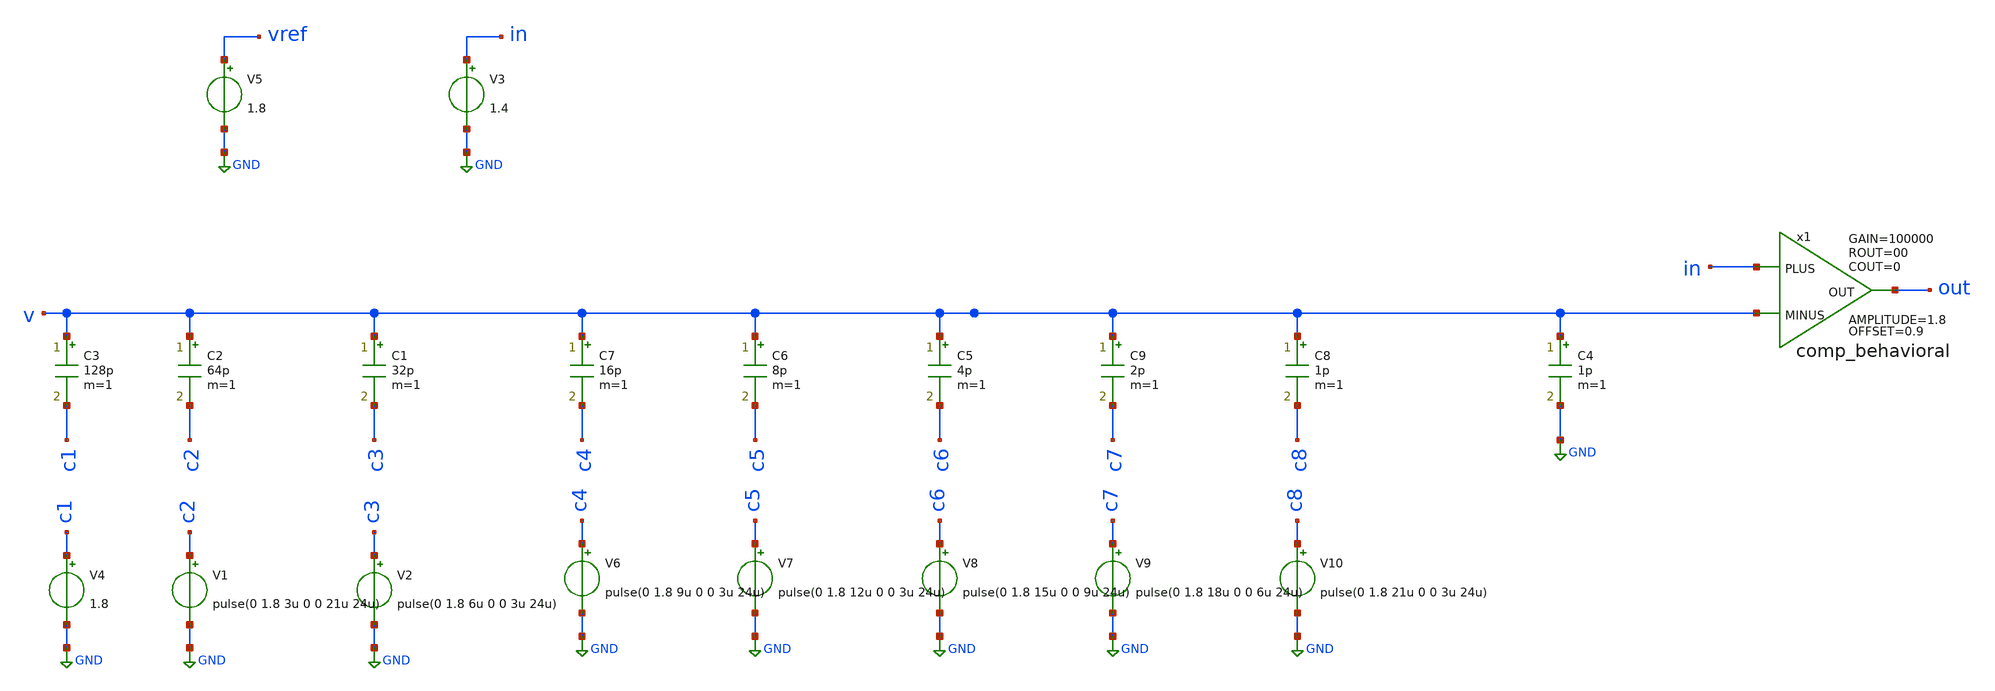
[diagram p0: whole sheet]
** sch_path: Behavioral_model/S_SARADC.sch
**.subckt S_SARADC
x1 in v out comp_behavioral OFFSET=0.9 AMPLITUDE=1.8 GAIN=100000 ROUT=00 COUT=0
V3 in GND 1.4
V4 c1 GND 1.8
C1 v c3 32p m=1
C2 v c2 64p m=1
C3 v c1 128p m=1
C4 v GND 1p m=1
V1 c2 GND pulse(0 1.8 3u 0 0 21u 24u)
V2 c3 GND pulse(0 1.8 6u 0 0 3u 24u)
V5 vref GND 1.8
C5 v c6 4p m=1
C6 v c5 8p m=1
C7 v c4 16p m=1
C8 v c8 1p m=1
C9 v c7 2p m=1
V6 c4 GND pulse(0 1.8 9u 0 0 3u 24u)
V7 c5 GND pulse(0 1.8 12u 0 0 3u 24u)
V8 c6 GND pulse(0 1.8 15u 0 0 9u 24u)
V9 c7 GND pulse(0 1.8 18u 0 0 6u 24u)
V10 c8 GND pulse(0 1.8 21u 0 0 3u 24u)
**** begin user architecture code

.tran 1n 24u
.save all
.control
plot c1; plot c2; plot c3; plot V
.endc


.lib /usr/local/share/pdk/sky130A/libs.tech/ngspice/sky130.lib.spice tt


.model switch1 sw vt=0.1 vh=0 ron=1m roff=100G

**** end user architecture code
**.ends

* expanding   symbol:  comp_behavioral.sym # of pins=3
** sym_path: Behavioral_model/comp_behavioral.sym
** sch_path: Behavioral_model/comp_behavioral.sch
.subckt comp_behavioral PLUS MINUS OUT  OFFSET=0.9 AMPLITUDE=0.9 GAIN=100000 ROUT=00 COUT=0
*.ipin PLUS
*.ipin MINUS
*.opin OUT
B1 IOUT 0 V = {OFFSET + AMPLITUDE/2*(tanh(V(IPLUS,IMINUS)*GAIN*2/AMPLITUDE))}
V1 IPLUS PLUS 3
V2 IMINUS MINUS 3
R1 OUT IOUT {ROUT} m=1
C3 OUT 0 {COUT} m=1
.ends

.GLOBAL GND
.end
